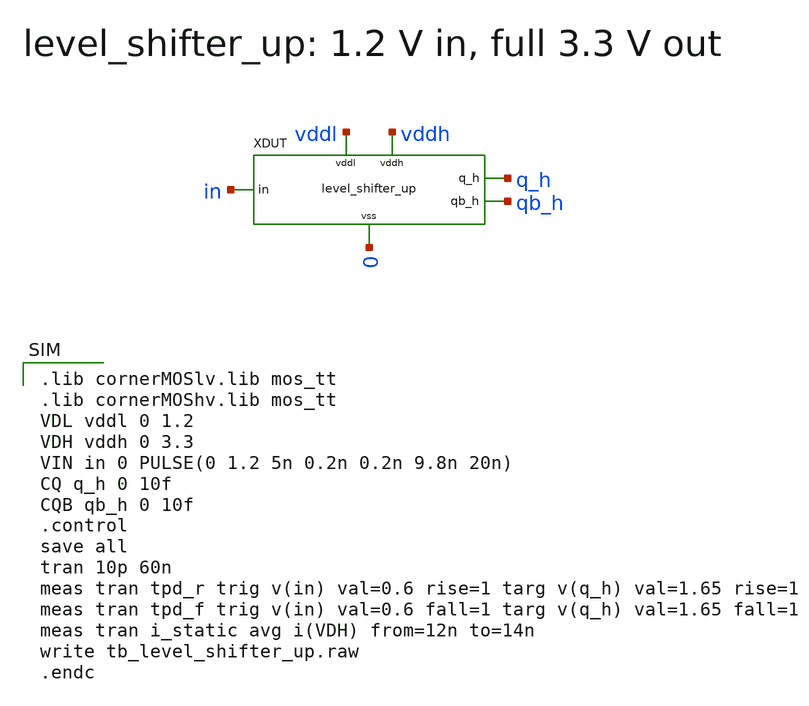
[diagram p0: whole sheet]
** sch_path: verification/tb_level_shifter_up.sch
**.subckt tb_level_shifter_up
XDUT in q_h qb_h vddl vddh 0 level_shifter_up
**** begin user architecture code

.lib cornerMOSlv.lib mos_tt
.lib cornerMOShv.lib mos_tt
VDL vddl 0 1.2
VDH vddh 0 3.3
VIN in 0 PULSE(0 1.2 5n 0.2n 0.2n 9.8n 20n)
CQ q_h 0 10f
CQB qb_h 0 10f
.control
save all
tran 10p 60n
meas tran tpd_r trig v(in) val=0.6 rise=1 targ v(q_h) val=1.65 rise=1
meas tran tpd_f trig v(in) val=0.6 fall=1 targ v(q_h) val=1.65 fall=1
meas tran i_static avg i(VDH) from=12n to=14n
write tb_level_shifter_up.raw
.endc

**** end user architecture code
**.ends
.end
